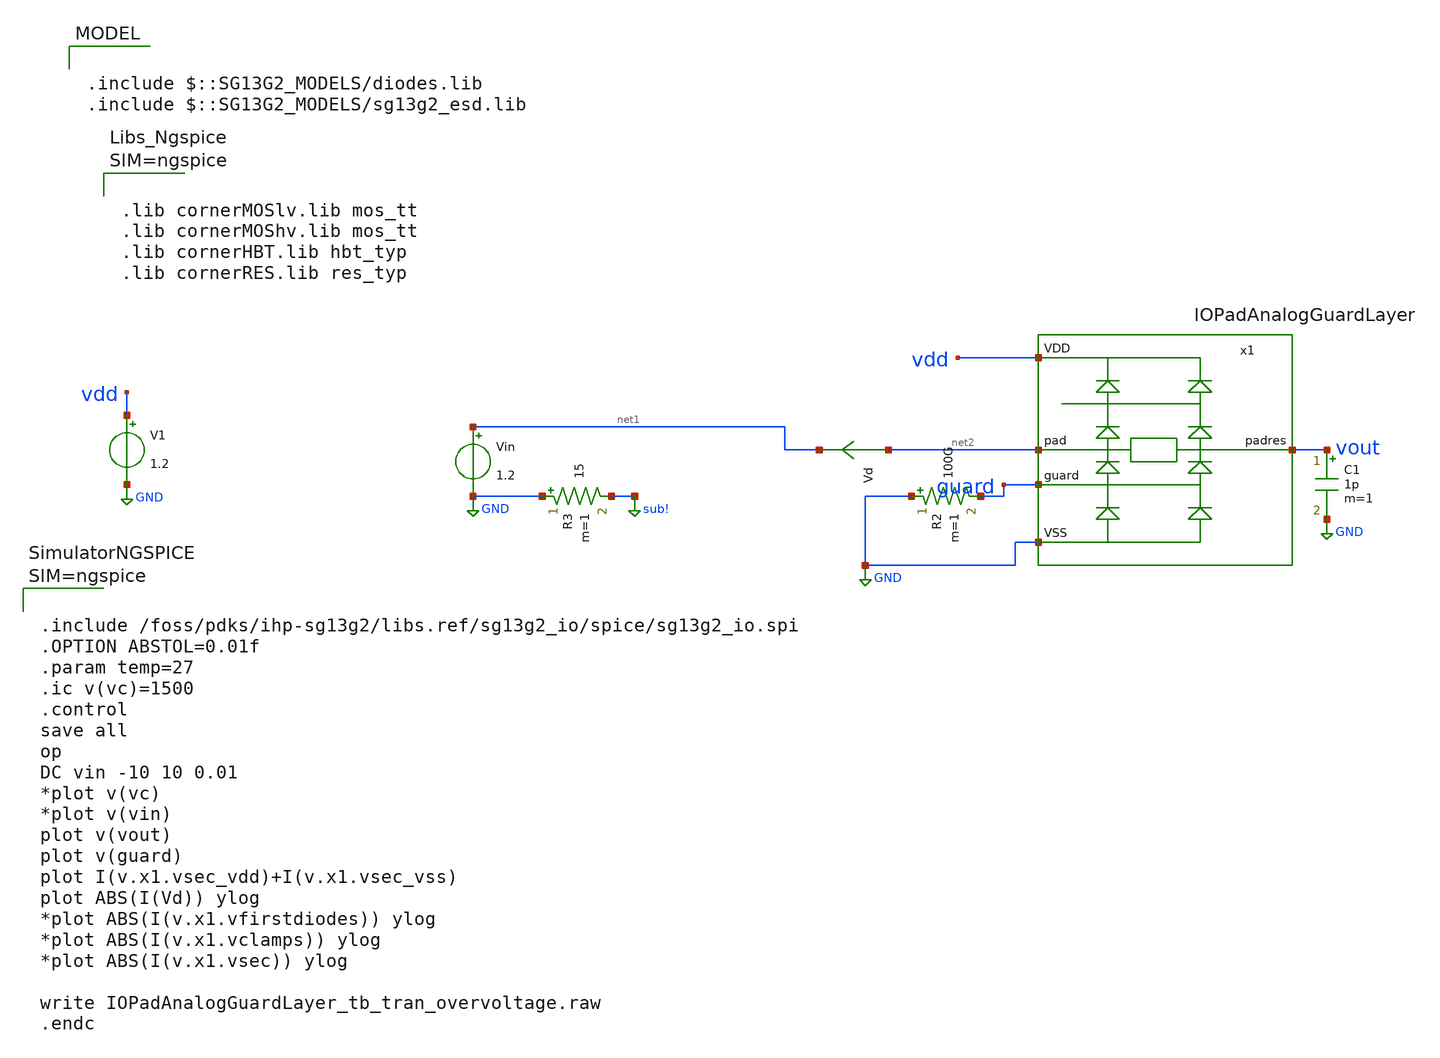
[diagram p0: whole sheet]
** sch_path: trident_test_structures/design_data/xschem/IOPadAnalogGuardLayer/IOPadAnalogGuardLayer_tb_tran_overvoltage.sch
**.subckt IOPadAnalogGuardLayer_tb_tran_overvoltage
V1 vdd GND 1.2
Vd net2 net1 0
.save i(vd)
C1 vout GND 1p m=1
R2 GND guard 100G m=1
R3 GND sub! 15 m=1
x1 vdd net2 vout guard GND IOPadAnalogGuardLayer
Vin net1 GND 1.2
**** begin user architecture code



.lib cornerMOSlv.lib mos_tt
.lib cornerMOShv.lib mos_tt
.lib cornerHBT.lib hbt_typ
.lib cornerRES.lib res_typ






.include /foss/pdks/ihp-sg13g2/libs.ref/sg13g2_io/spice/sg13g2_io.spi
.OPTION ABSTOL=0.01f
.param temp=27
.ic v(vc)=1500
.control
save all
op
DC vin -10 10 0.01
*plot v(vc)
*plot v(vin)
plot v(vout)
plot v(guard)
plot I(v.x1.vsec_vdd)+I(v.x1.vsec_vss)
plot ABS(I(Vd)) ylog
*plot ABS(I(v.x1.vfirstdiodes)) ylog
*plot ABS(I(v.x1.vclamps)) ylog
*plot ABS(I(v.x1.vsec)) ylog

write IOPadAnalogGuardLayer_tb_tran_overvoltage.raw
.endc




.include $::SG13G2_MODELS/diodes.lib
.include $::SG13G2_MODELS/sg13g2_esd.lib

**** end user architecture code
**.ends
.GLOBAL GND
.GLOBAL sub!
.end
